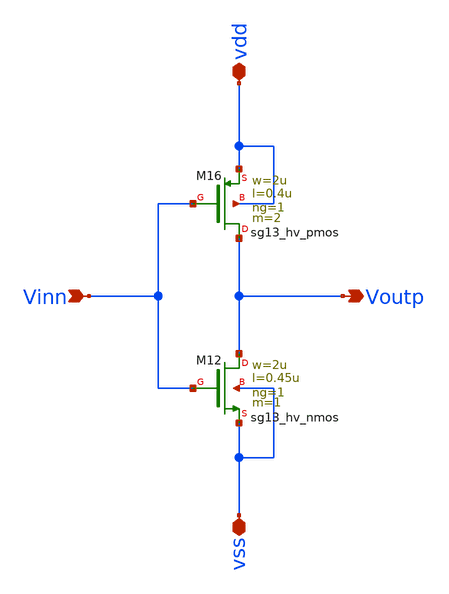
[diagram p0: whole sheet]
** sch_path: circuit_files/sar_adc_test/xschem/inverter.sch
**.subckt inverter vdd vss Vinn Voutp
*.iopin vdd
*.iopin vss
*.ipin Vinn
*.opin Voutp
XM12 Voutp Vinn vss vss sg13_hv_nmos w=2u l=0.45u ng=1 m=1 mm_ok=1
XM16 Voutp Vinn vdd vdd sg13_hv_pmos w=2u l=0.4u ng=1 m=2 mm_ok=1
**.ends
.end
